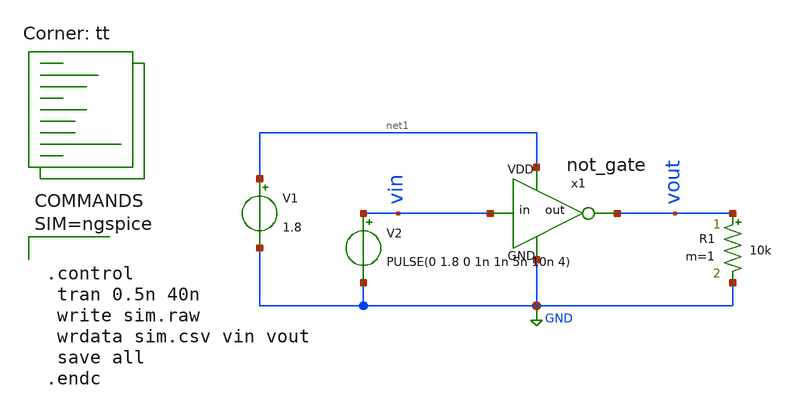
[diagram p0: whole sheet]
** sch_path: tp6/inversor.sky130/simulation/sim.sch
**.subckt sim
V1 net1 GND 1.8
V2 vin GND PULSE(0 1.8 0 1n 1n 5n 10n 4)
R1 vout GND 10k m=1
x1 vout vin GND net1 not_gate
**** begin user architecture code
.lib $::SKYWATER_MODELS/sky130.lib.spice tt



.control
 tran 0.5n 40n
 write sim.raw
 wrdata sim.csv vin vout
 save all
.endc



**** end user architecture code
**.ends
.GLOBAL GND
.end
